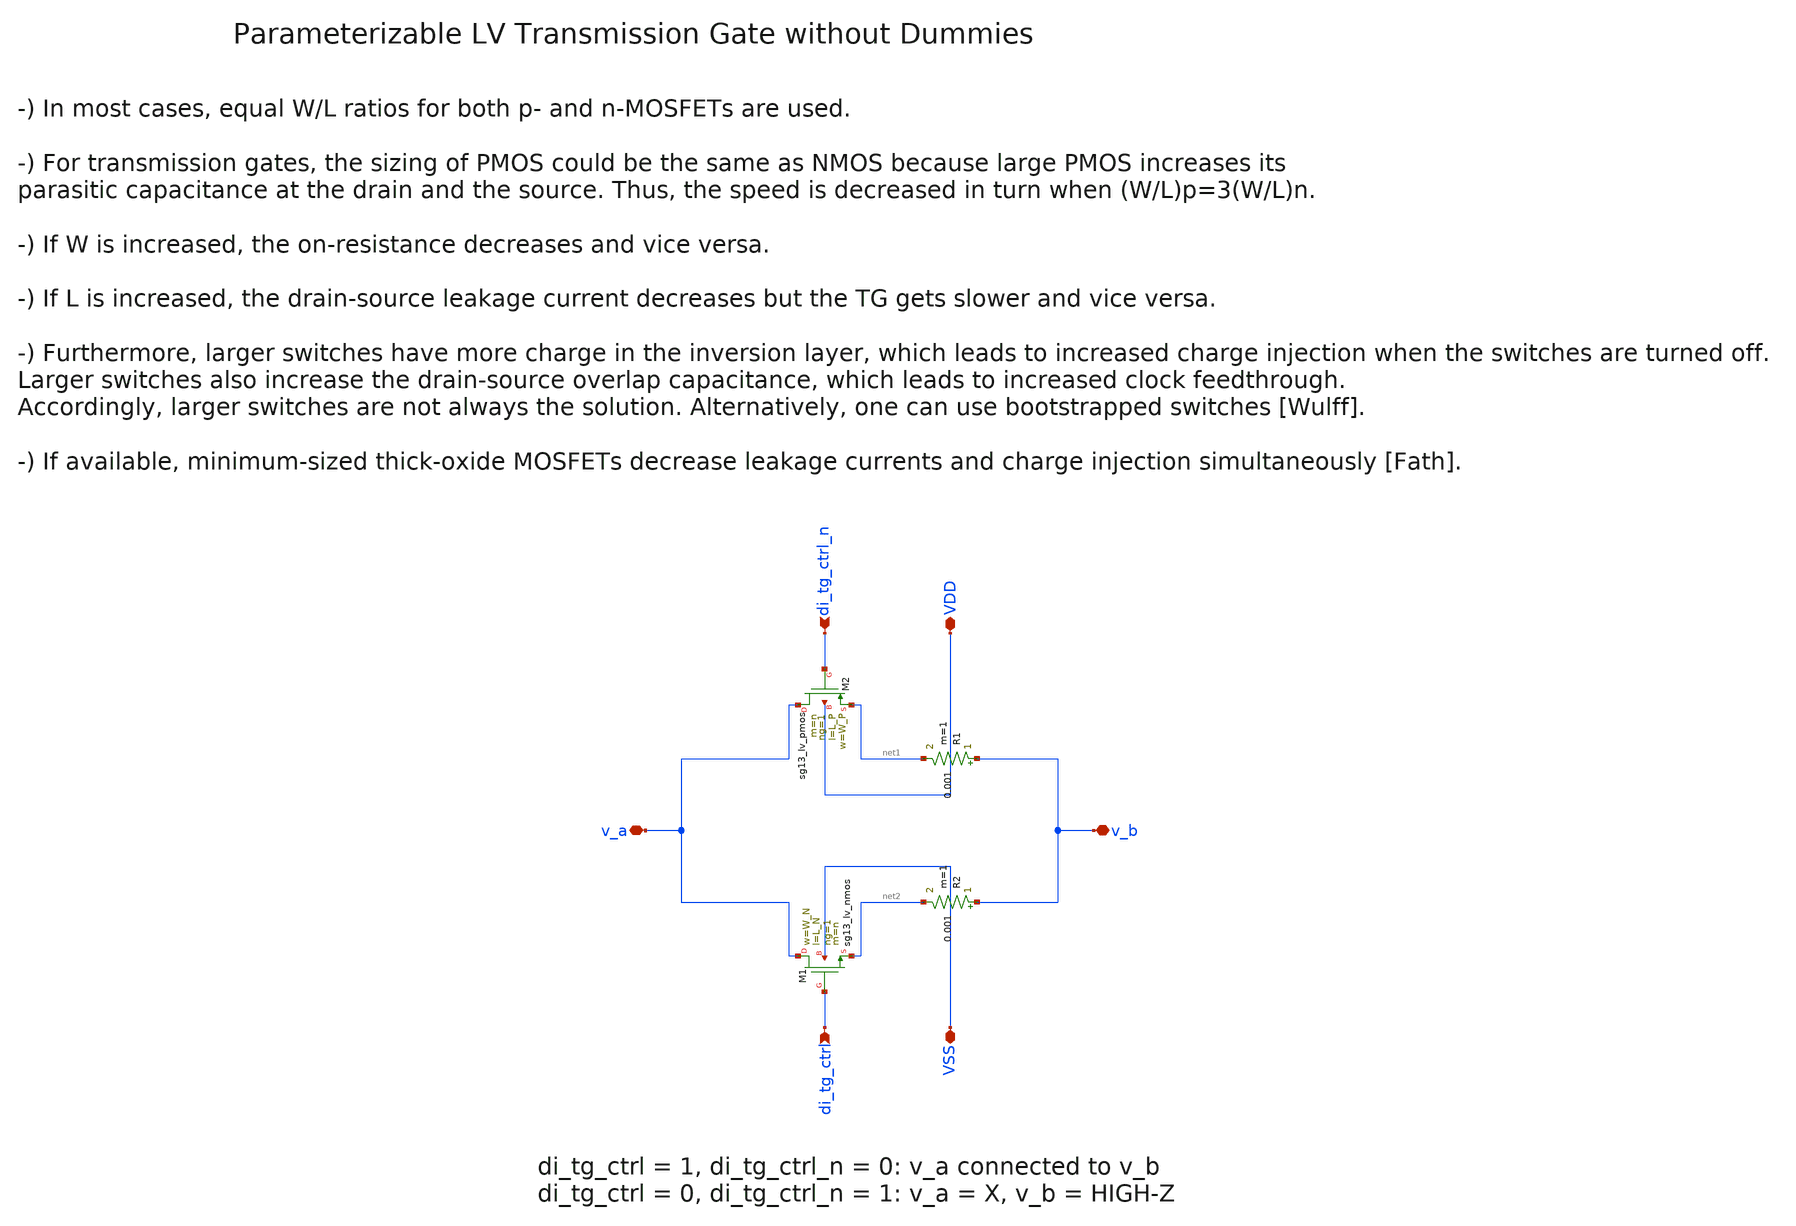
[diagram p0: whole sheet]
** sch_path: xschem/transmission_gate/transmission_gate_lv_wo_dummy.sch
**.subckt transmission_gate_lv_wo_dummy v_a v_b VDD VSS di_tg_ctrl di_tg_ctrl_n
*.iopin v_a
*.iopin v_b
*.iopin VDD
*.iopin VSS
*.ipin di_tg_ctrl
*.ipin di_tg_ctrl_n
XM1 v_a di_tg_ctrl net2 VSS sg13_lv_nmos w=W_N l=L_N ng=1 m=n mm_ok=1
XM2 v_a di_tg_ctrl_n net1 VDD sg13_lv_pmos w=W_P l=L_P ng=1 m=n mm_ok=1
R1 v_b net1 0.001 m=1
R2 v_b net2 0.001 m=1
**.ends
.end
